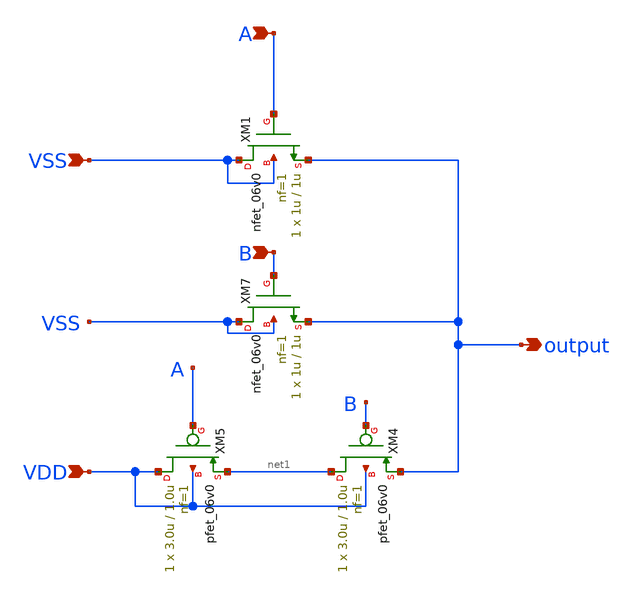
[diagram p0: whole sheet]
** sch_path: FINAL/XSCHEM/DECODER/nor.sch
**.subckt nor VSS B A output VDD
*.ipin VSS
*.ipin B
*.ipin A
*.opin output
*.ipin VDD
XM4 net1 B output VDD pfet_06v0 L=1.0u W=3.0u nf=1 ad='int((nf+1)/2) * W/nf * 0.18u' as='int((nf+2)/2) * W/nf * 0.18u'
+ pd='2*int((nf+1)/2) * (W/nf + 0.18u)' ps='2*int((nf+2)/2) * (W/nf + 0.18u)' nrd='0.18u / W' nrs='0.18u / W'
+ sa=0 sb=0 sd=0 m=1
XM5 VDD A net1 VDD pfet_06v0 L=1.0u W=3.0u nf=1 ad='int((nf+1)/2) * W/nf * 0.18u' as='int((nf+2)/2) * W/nf * 0.18u'
+ pd='2*int((nf+1)/2) * (W/nf + 0.18u)' ps='2*int((nf+2)/2) * (W/nf + 0.18u)' nrd='0.18u / W' nrs='0.18u / W'
+ sa=0 sb=0 sd=0 m=1
XM7 VSS B output VSS nfet_06v0 L=1u W=1u nf=1 ad='int((nf+1)/2) * W/nf * 0.18u' as='int((nf+2)/2) * W/nf * 0.18u'
+ pd='2*int((nf+1)/2) * (W/nf + 0.18u)' ps='2*int((nf+2)/2) * (W/nf + 0.18u)' nrd='0.18u / W' nrs='0.18u / W'
+ sa=0 sb=0 sd=0 m=1
XM1 VSS A output VSS nfet_06v0 L=1u W=1u nf=1 ad='int((nf+1)/2) * W/nf * 0.18u' as='int((nf+2)/2) * W/nf * 0.18u'
+ pd='2*int((nf+1)/2) * (W/nf + 0.18u)' ps='2*int((nf+2)/2) * (W/nf + 0.18u)' nrd='0.18u / W' nrs='0.18u / W'
+ sa=0 sb=0 sd=0 m=1
**.ends
.end
